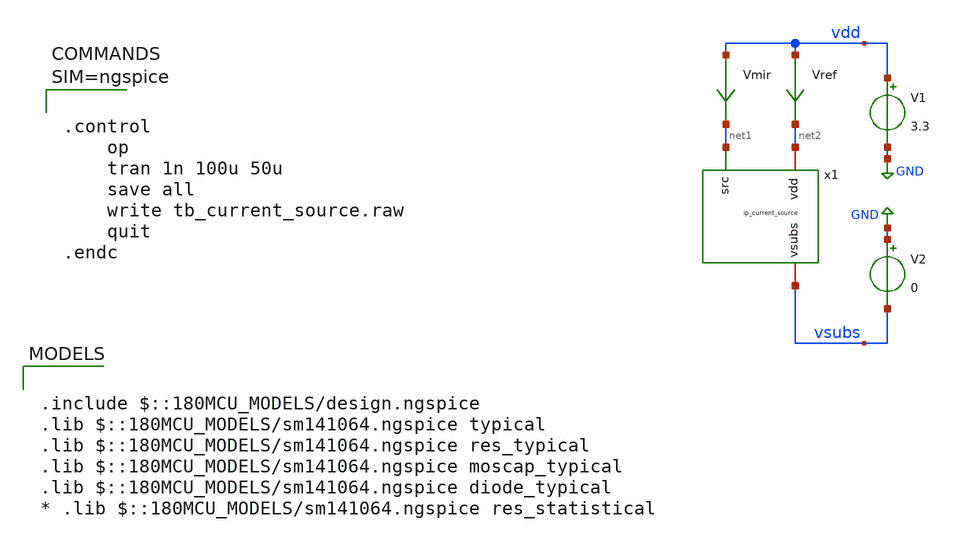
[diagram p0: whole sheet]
** sch_path: xschem/tb_current_source.sch
**.subckt tb_current_source
x1 net2 net1 vsubs ip_current_source
V1 vdd GND 3.3
V2 GND vsubs 0
Vmir vdd net1 0
.save i(vmir)
Vref vdd net2 0
.save i(vref)
**** begin user architecture code

.include $::180MCU_MODELS/design.ngspice
.lib $::180MCU_MODELS/sm141064.ngspice typical
.lib $::180MCU_MODELS/sm141064.ngspice res_typical
.lib $::180MCU_MODELS/sm141064.ngspice moscap_typical
.lib $::180MCU_MODELS/sm141064.ngspice diode_typical
* .lib $::180MCU_MODELS/sm141064.ngspice res_statistical




.control
	op
	tran 1n 100u 50u
	save all
	write tb_current_source.raw
	quit
.endc



**** end user architecture code
**.ends

* expanding   symbol:  ip_current_source.sym # of pins=3
** sym_path: xschem/ip_current_source.sym
** sch_path: xschem/ip_current_source.sch
.subckt ip_current_source vdd src vsubs
*.iopin vdd
*.iopin vsubs
*.ipin src
XM1 net1 net1 vsubs vsubs nfet_03v3 L=1u W=5u nf=1 ad='int((nf+1)/2) * W/nf * 0.18u' as='int((nf+2)/2) * W/nf * 0.18u'
+ pd='2*int((nf+1)/2) * (W/nf + 0.18u)' ps='2*int((nf+2)/2) * (W/nf + 0.18u)' nrd='0.18u / W' nrs='0.18u / W'
+ sa=0 sb=0 sd=0 m=1
XM2 src net1 vsubs vsubs nfet_03v3 L=2u W=0.5u nf=1 ad='int((nf+1)/2) * W/nf * 0.18u' as='int((nf+2)/2) * W/nf * 0.18u'
+ pd='2*int((nf+1)/2) * (W/nf + 0.18u)' ps='2*int((nf+2)/2) * (W/nf + 0.18u)' nrd='0.18u / W' nrs='0.18u / W'
+ sa=0 sb=0 sd=0 m=1
XR2 net1 vdd vsubs ppolyf_u_3k r_width=1e-6 r_length=10e-6 m=1
.ends

.GLOBAL GND
.end
